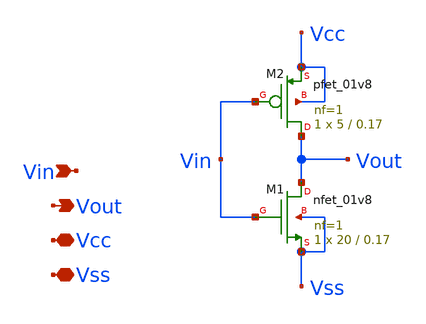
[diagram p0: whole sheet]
** sch_path: Git Files/Schematic/Pre Emphasis Driver/Buf2/inv22.sch
**.subckt inv22 Vin Vout Vcc Vss
*.ipin Vin
*.opin Vout
*.iopin Vcc
*.iopin Vss
XM1 Vout Vin Vss Vss sky130_fd_pr__nfet_01v8 L=0.17 W=20 nf=1 ad='int((nf+1)/2) * W/nf * 0.29' as='int((nf+2)/2) * W/nf * 0.29'
+ pd='2*int((nf+1)/2) * (W/nf + 0.29)' ps='2*int((nf+2)/2) * (W/nf + 0.29)' nrd='0.29 / W' nrs='0.29 / W'
+ sa=0 sb=0 sd=0 mult=1 m=1
XM2 Vout Vin Vcc Vcc sky130_fd_pr__pfet_01v8 L=0.17 W=5 nf=1 ad='int((nf+1)/2) * W/nf * 0.29' as='int((nf+2)/2) * W/nf * 0.29'
+ pd='2*int((nf+1)/2) * (W/nf + 0.29)' ps='2*int((nf+2)/2) * (W/nf + 0.29)' nrd='0.29 / W' nrs='0.29 / W'
+ sa=0 sb=0 sd=0 mult=1 m=1
**.ends
.end
